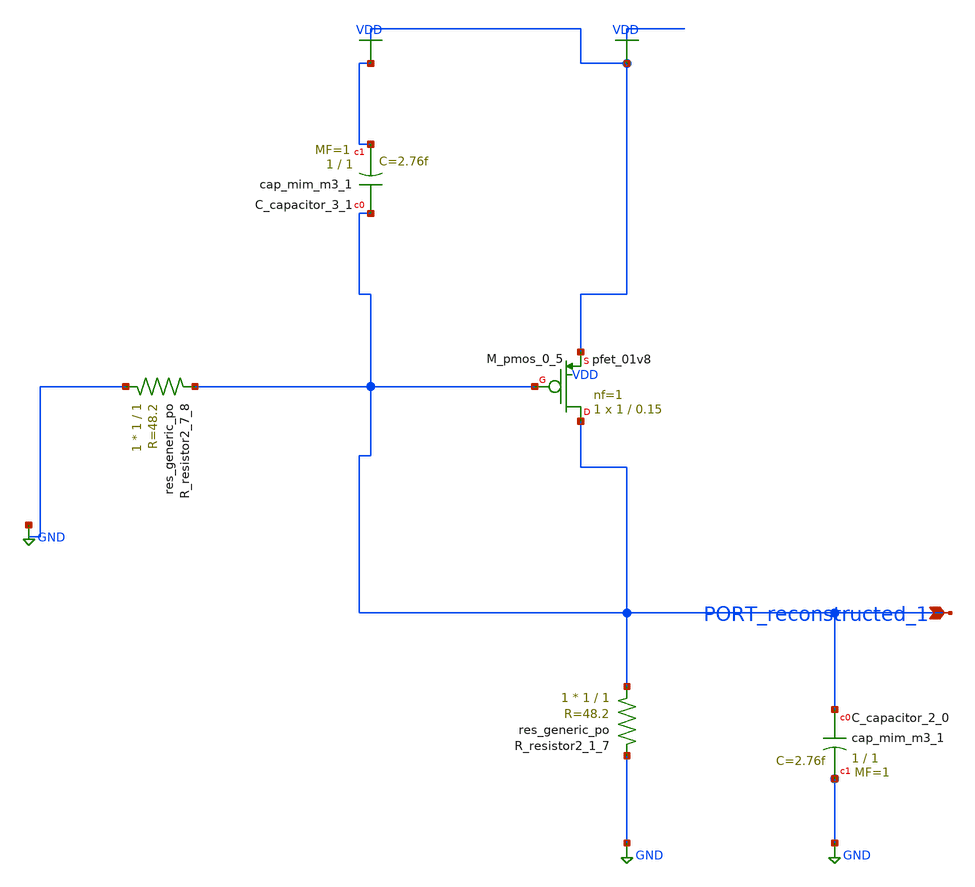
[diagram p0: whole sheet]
** sch_path: schematics/AMSNet/723.sch
**.subckt 723 PORT_reconstructed_1
*.ipin PORT_reconstructed_1
XC_capacitor_2_0 PORT_reconstructed_1 GND sky130_fd_pr__cap_mim_m3_1 W=1 L=1 MF=1 m=1
XC_capacitor_3_1 PORT_reconstructed_1 VDD sky130_fd_pr__cap_mim_m3_1 W=1 L=1 MF=1 m=1
XM_pmos_0_5 PORT_reconstructed_1 PORT_reconstructed_1 VDD VDD sky130_fd_pr__pfet_01v8 L=0.15 W=1 nf=1
+ ad='int((1 + 1)/2) * 1 / 1 * 0.29' as='int((1 + 2)/2) * 1 / 1 * 0.29' pd='2*int((1 + 1)/2) * (1 / 1 + 0.29)'
+ ps='2*int((1 + 2)/2) * (1 / 1 + 0.29)' nrd='0.29 / 1 ' nrs='0.29 / 1 ' sa=0 sb=0 sd=0 mult=1 m=1
XR_resistor2_1_7 PORT_reconstructed_1 GND sky130_fd_pr__res_generic_po W=1 L=1 m=1
XR_resistor2_7_8 GND PORT_reconstructed_1 sky130_fd_pr__res_generic_po W=1 L=1 m=1
**.ends
.GLOBAL GND
.GLOBAL VDD
.end
